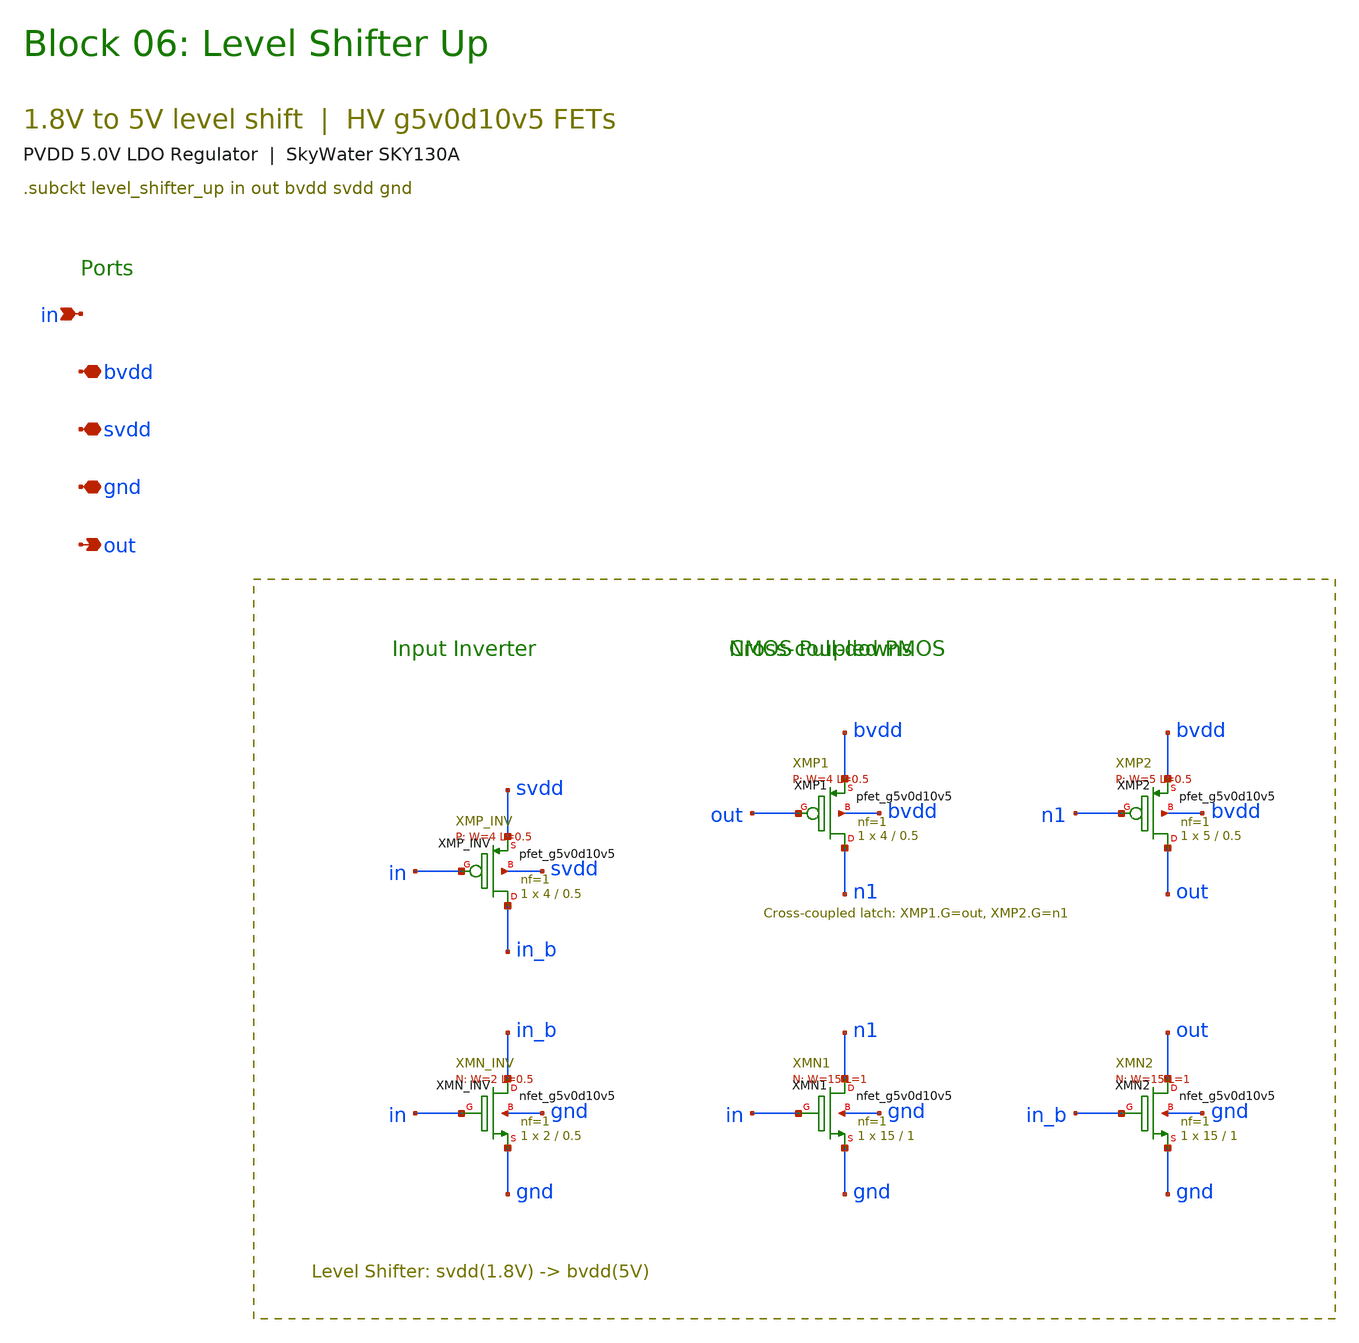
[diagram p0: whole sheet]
** sch_path: pvdd_regulator/10_top_integration/schematics/pvdd_06_level_shifter.sch
**.subckt pvdd_06_level_shifter in bvdd svdd gnd out
*.ipin in
*.iopin bvdd
*.iopin svdd
*.iopin gnd
*.opin out
XXMN_INV in_b in gnd gnd sky130_fd_pr__nfet_g5v0d10v5 L=0.5 W=2 nf=1 ad='int((1 + 1)/2) * 2 / 1 * 0.29'
+ as='int((1 + 2)/2) * 2 / 1 * 0.29' pd='2*int((1 + 1)/2) * (2 / 1 + 0.29)' ps='2*int((1 + 2)/2) * (2 / 1 + 0.29)'
+ nrd='0.29 / 2 ' nrs='0.29 / 2 ' sa=0 sb=0 sd=0 mult=1 m=1
XXMP_INV in_b in svdd svdd sky130_fd_pr__pfet_g5v0d10v5 L=0.5 W=4 nf=1 ad='int((1 + 1)/2) * 4 / 1 * 0.29'
+ as='int((1 + 2)/2) * 4 / 1 * 0.29' pd='2*int((1 + 1)/2) * (4 / 1 + 0.29)' ps='2*int((1 + 2)/2) * (4 / 1 + 0.29)'
+ nrd='0.29 / 4 ' nrs='0.29 / 4 ' sa=0 sb=0 sd=0 mult=1 m=1
XXMN1 n1 in gnd gnd sky130_fd_pr__nfet_g5v0d10v5 L=1 W=15 nf=1 ad='int((1 + 1)/2) * 15 / 1 * 0.29' as='int((1 + 2)/2) * 15 / 1 * 0.29'
+ pd='2*int((1 + 1)/2) * (15 / 1 + 0.29)' ps='2*int((1 + 2)/2) * (15 / 1 + 0.29)' nrd='0.29 / 15 ' nrs='0.29 / 15 '
+ sa=0 sb=0 sd=0 mult=1 m=1
XXMN2 out in_b gnd gnd sky130_fd_pr__nfet_g5v0d10v5 L=1 W=15 nf=1 ad='int((1 + 1)/2) * 15 / 1 * 0.29'
+ as='int((1 + 2)/2) * 15 / 1 * 0.29' pd='2*int((1 + 1)/2) * (15 / 1 + 0.29)' ps='2*int((1 + 2)/2) * (15 / 1 + 0.29)'
+ nrd='0.29 / 15 ' nrs='0.29 / 15 ' sa=0 sb=0 sd=0 mult=1 m=1
XXMP1 n1 out bvdd bvdd sky130_fd_pr__pfet_g5v0d10v5 L=0.5 W=4 nf=1 ad='int((1 + 1)/2) * 4 / 1 * 0.29'
+ as='int((1 + 2)/2) * 4 / 1 * 0.29' pd='2*int((1 + 1)/2) * (4 / 1 + 0.29)' ps='2*int((1 + 2)/2) * (4 / 1 + 0.29)'
+ nrd='0.29 / 4 ' nrs='0.29 / 4 ' sa=0 sb=0 sd=0 mult=1 m=1
XXMP2 out n1 bvdd bvdd sky130_fd_pr__pfet_g5v0d10v5 L=0.5 W=5 nf=1 ad='int((1 + 1)/2) * 5 / 1 * 0.29'
+ as='int((1 + 2)/2) * 5 / 1 * 0.29' pd='2*int((1 + 1)/2) * (5 / 1 + 0.29)' ps='2*int((1 + 2)/2) * (5 / 1 + 0.29)'
+ nrd='0.29 / 5 ' nrs='0.29 / 5 ' sa=0 sb=0 sd=0 mult=1 m=1
**.ends
.end
